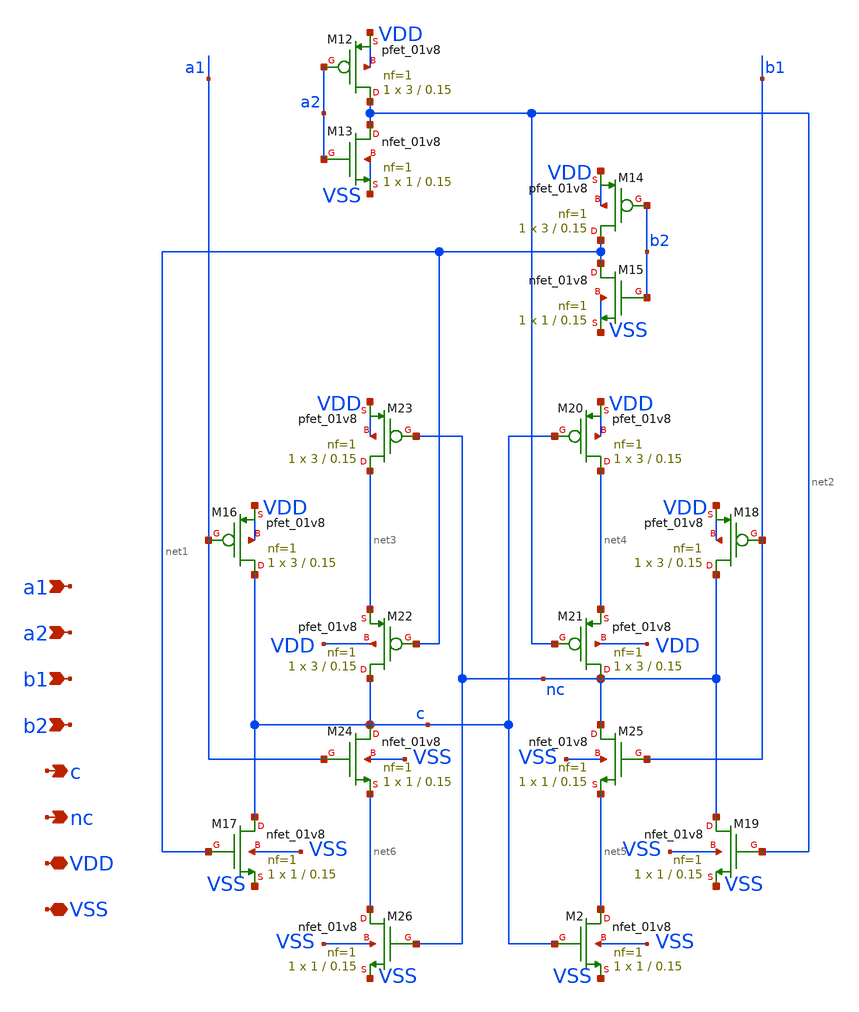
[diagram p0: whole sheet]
** sch_path: xschem/saff_bottom_latch.sch
**.subckt saff_bottom_latch VDD a1 c VSS b2 nc a2 b1
*.iopin VDD
*.ipin a1
*.opin c
*.iopin VSS
*.ipin b2
*.opin nc
*.ipin a2
*.ipin b1
XM2 net5 c VSS VSS sky130_fd_pr__nfet_01v8 L=0.15 W=1 nf=1 ad='int((nf+1)/2) * W/nf * 0.29' as='int((nf+2)/2) * W/nf * 0.29'
+ pd='2*int((nf+1)/2) * (W/nf + 0.29)' ps='2*int((nf+2)/2) * (W/nf + 0.29)' nrd='0.29 / W' nrs='0.29 / W'
+ sa=0 sb=0 sd=0 mult=1 m=1
XM12 net2 a2 VDD VDD sky130_fd_pr__pfet_01v8 L=0.15 W=3 nf=1 ad='int((nf+1)/2) * W/nf * 0.29' as='int((nf+2)/2) * W/nf * 0.29'
+ pd='2*int((nf+1)/2) * (W/nf + 0.29)' ps='2*int((nf+2)/2) * (W/nf + 0.29)' nrd='0.29 / W' nrs='0.29 / W'
+ sa=0 sb=0 sd=0 mult=1 m=1
XM13 net2 a2 VSS VSS sky130_fd_pr__nfet_01v8 L=0.15 W=1 nf=1 ad='int((nf+1)/2) * W/nf * 0.29' as='int((nf+2)/2) * W/nf * 0.29'
+ pd='2*int((nf+1)/2) * (W/nf + 0.29)' ps='2*int((nf+2)/2) * (W/nf + 0.29)' nrd='0.29 / W' nrs='0.29 / W'
+ sa=0 sb=0 sd=0 mult=1 m=1
XM14 net1 b2 VDD VDD sky130_fd_pr__pfet_01v8 L=0.15 W=3 nf=1 ad='int((nf+1)/2) * W/nf * 0.29' as='int((nf+2)/2) * W/nf * 0.29'
+ pd='2*int((nf+1)/2) * (W/nf + 0.29)' ps='2*int((nf+2)/2) * (W/nf + 0.29)' nrd='0.29 / W' nrs='0.29 / W'
+ sa=0 sb=0 sd=0 mult=1 m=1
XM15 net1 b2 VSS VSS sky130_fd_pr__nfet_01v8 L=0.15 W=1 nf=1 ad='int((nf+1)/2) * W/nf * 0.29' as='int((nf+2)/2) * W/nf * 0.29'
+ pd='2*int((nf+1)/2) * (W/nf + 0.29)' ps='2*int((nf+2)/2) * (W/nf + 0.29)' nrd='0.29 / W' nrs='0.29 / W'
+ sa=0 sb=0 sd=0 mult=1 m=1
XM16 c a1 VDD VDD sky130_fd_pr__pfet_01v8 L=0.15 W=3 nf=1 ad='int((nf+1)/2) * W/nf * 0.29' as='int((nf+2)/2) * W/nf * 0.29'
+ pd='2*int((nf+1)/2) * (W/nf + 0.29)' ps='2*int((nf+2)/2) * (W/nf + 0.29)' nrd='0.29 / W' nrs='0.29 / W'
+ sa=0 sb=0 sd=0 mult=1 m=1
XM17 c net1 VSS VSS sky130_fd_pr__nfet_01v8 L=0.15 W=1 nf=1 ad='int((nf+1)/2) * W/nf * 0.29' as='int((nf+2)/2) * W/nf * 0.29'
+ pd='2*int((nf+1)/2) * (W/nf + 0.29)' ps='2*int((nf+2)/2) * (W/nf + 0.29)' nrd='0.29 / W' nrs='0.29 / W'
+ sa=0 sb=0 sd=0 mult=1 m=1
XM18 nc b1 VDD VDD sky130_fd_pr__pfet_01v8 L=0.15 W=3 nf=1 ad='int((nf+1)/2) * W/nf * 0.29' as='int((nf+2)/2) * W/nf * 0.29'
+ pd='2*int((nf+1)/2) * (W/nf + 0.29)' ps='2*int((nf+2)/2) * (W/nf + 0.29)' nrd='0.29 / W' nrs='0.29 / W'
+ sa=0 sb=0 sd=0 mult=1 m=1
XM19 nc net2 VSS VSS sky130_fd_pr__nfet_01v8 L=0.15 W=1 nf=1 ad='int((nf+1)/2) * W/nf * 0.29' as='int((nf+2)/2) * W/nf * 0.29'
+ pd='2*int((nf+1)/2) * (W/nf + 0.29)' ps='2*int((nf+2)/2) * (W/nf + 0.29)' nrd='0.29 / W' nrs='0.29 / W'
+ sa=0 sb=0 sd=0 mult=1 m=1
XM20 net4 c VDD VDD sky130_fd_pr__pfet_01v8 L=0.15 W=3 nf=1 ad='int((nf+1)/2) * W/nf * 0.29' as='int((nf+2)/2) * W/nf * 0.29'
+ pd='2*int((nf+1)/2) * (W/nf + 0.29)' ps='2*int((nf+2)/2) * (W/nf + 0.29)' nrd='0.29 / W' nrs='0.29 / W'
+ sa=0 sb=0 sd=0 mult=1 m=1
XM21 nc net2 net4 VDD sky130_fd_pr__pfet_01v8 L=0.15 W=3 nf=1 ad='int((nf+1)/2) * W/nf * 0.29' as='int((nf+2)/2) * W/nf * 0.29'
+ pd='2*int((nf+1)/2) * (W/nf + 0.29)' ps='2*int((nf+2)/2) * (W/nf + 0.29)' nrd='0.29 / W' nrs='0.29 / W'
+ sa=0 sb=0 sd=0 mult=1 m=1
XM22 c net1 net3 VDD sky130_fd_pr__pfet_01v8 L=0.15 W=3 nf=1 ad='int((nf+1)/2) * W/nf * 0.29' as='int((nf+2)/2) * W/nf * 0.29'
+ pd='2*int((nf+1)/2) * (W/nf + 0.29)' ps='2*int((nf+2)/2) * (W/nf + 0.29)' nrd='0.29 / W' nrs='0.29 / W'
+ sa=0 sb=0 sd=0 mult=1 m=1
XM23 net3 nc VDD VDD sky130_fd_pr__pfet_01v8 L=0.15 W=3 nf=1 ad='int((nf+1)/2) * W/nf * 0.29' as='int((nf+2)/2) * W/nf * 0.29'
+ pd='2*int((nf+1)/2) * (W/nf + 0.29)' ps='2*int((nf+2)/2) * (W/nf + 0.29)' nrd='0.29 / W' nrs='0.29 / W'
+ sa=0 sb=0 sd=0 mult=1 m=1
XM24 c a1 net6 VSS sky130_fd_pr__nfet_01v8 L=0.15 W=1 nf=1 ad='int((nf+1)/2) * W/nf * 0.29' as='int((nf+2)/2) * W/nf * 0.29'
+ pd='2*int((nf+1)/2) * (W/nf + 0.29)' ps='2*int((nf+2)/2) * (W/nf + 0.29)' nrd='0.29 / W' nrs='0.29 / W'
+ sa=0 sb=0 sd=0 mult=1 m=1
XM25 nc b1 net5 VSS sky130_fd_pr__nfet_01v8 L=0.15 W=1 nf=1 ad='int((nf+1)/2) * W/nf * 0.29' as='int((nf+2)/2) * W/nf * 0.29'
+ pd='2*int((nf+1)/2) * (W/nf + 0.29)' ps='2*int((nf+2)/2) * (W/nf + 0.29)' nrd='0.29 / W' nrs='0.29 / W'
+ sa=0 sb=0 sd=0 mult=1 m=1
XM26 net6 nc VSS VSS sky130_fd_pr__nfet_01v8 L=0.15 W=1 nf=1 ad='int((nf+1)/2) * W/nf * 0.29' as='int((nf+2)/2) * W/nf * 0.29'
+ pd='2*int((nf+1)/2) * (W/nf + 0.29)' ps='2*int((nf+2)/2) * (W/nf + 0.29)' nrd='0.29 / W' nrs='0.29 / W'
+ sa=0 sb=0 sd=0 mult=1 m=1
**.ends
.end
